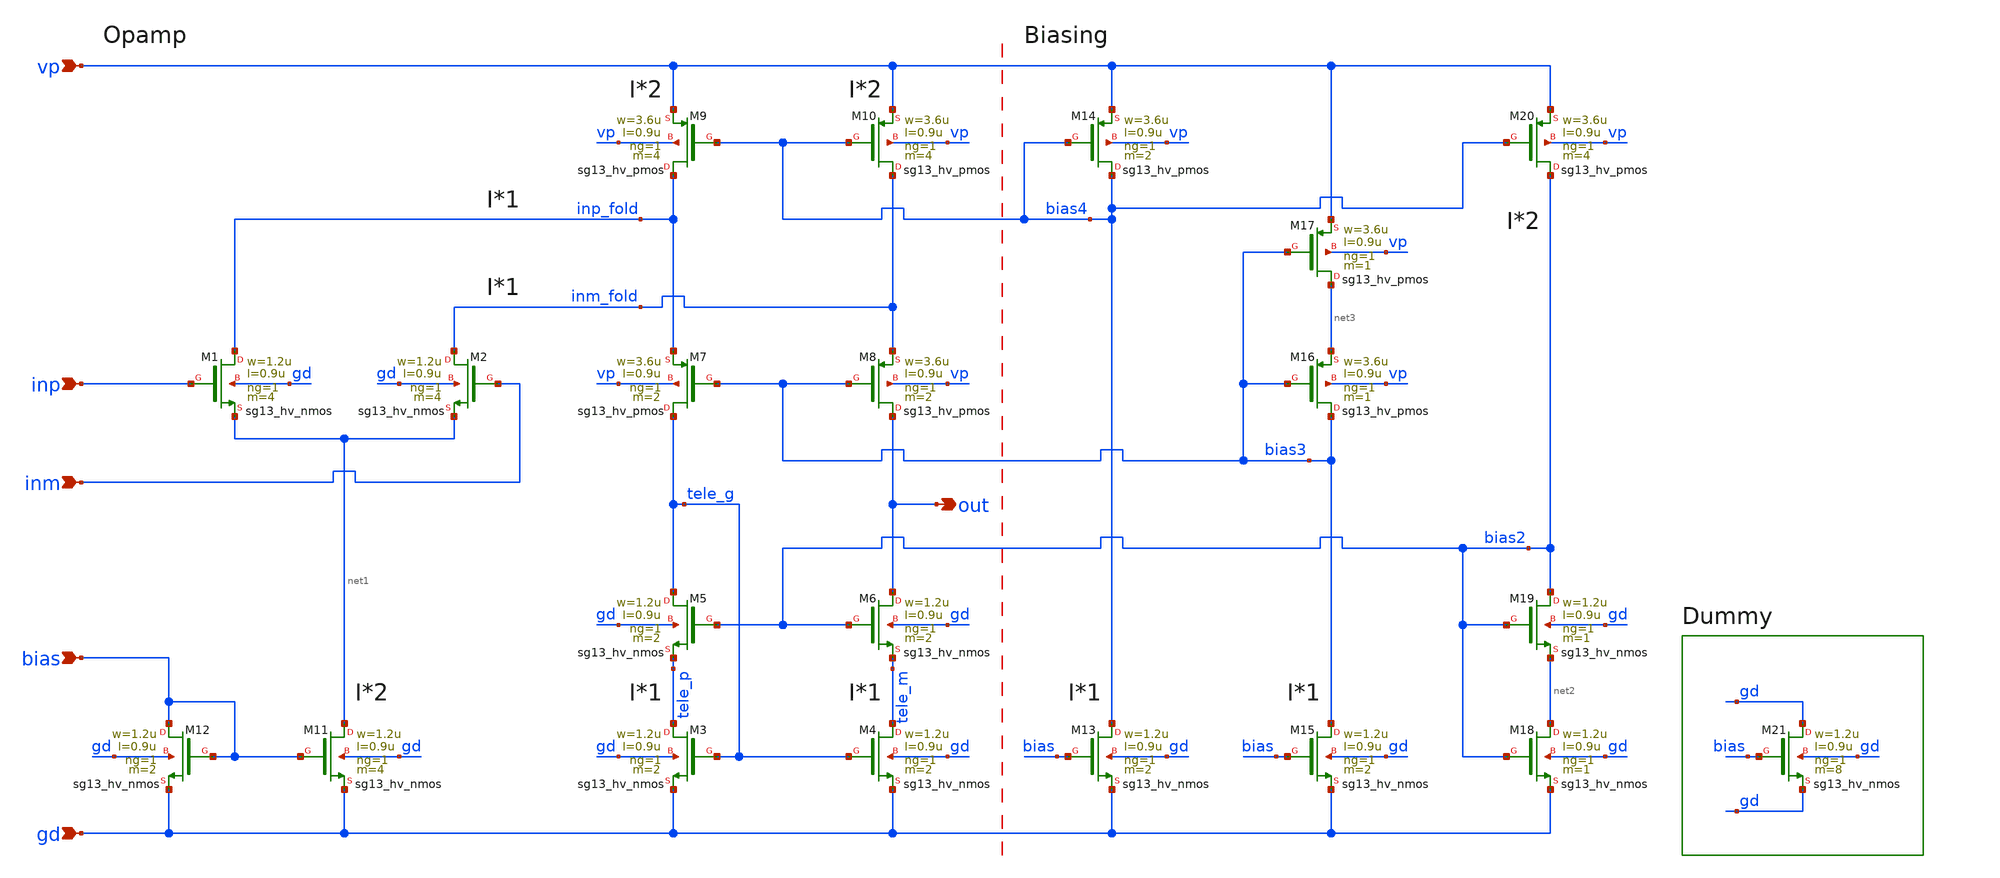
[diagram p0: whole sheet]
** sch_path: bandgap_res/opamp_folded.sch
**.subckt opamp_folded bias out vp inp inm gd
*.ipin bias
*.opin out
*.ipin vp
*.ipin inp
*.ipin inm
*.ipin gd
XM1 inp_fold inp net1 gd sg13_hv_nmos w=1.2u l=0.9u ng=1 m=4 mm_ok=1
XM2 inm_fold inm net1 gd sg13_hv_nmos w=1.2u l=0.9u ng=1 m=4 mm_ok=1
XM3 tele_p tele_g gd gd sg13_hv_nmos w=1.2u l=0.9u ng=1 m=2 mm_ok=1
XM4 tele_m tele_g gd gd sg13_hv_nmos w=1.2u l=0.9u ng=1 m=2 mm_ok=1
XM5 tele_g bias2 tele_p gd sg13_hv_nmos w=1.2u l=0.9u ng=1 m=2 mm_ok=1
XM6 out bias2 tele_m gd sg13_hv_nmos w=1.2u l=0.9u ng=1 m=2 mm_ok=1
XM7 tele_g bias3 inp_fold vp sg13_hv_pmos w=3.6u l=0.9u ng=1 m=2 mm_ok=1
XM8 out bias3 inm_fold vp sg13_hv_pmos w=3.6u l=0.9u ng=1 m=2 mm_ok=1
XM9 inp_fold bias4 vp vp sg13_hv_pmos w=3.6u l=0.9u ng=1 m=4 mm_ok=1
XM10 inm_fold bias4 vp vp sg13_hv_pmos w=3.6u l=0.9u ng=1 m=4 mm_ok=1
XM11 net1 bias gd gd sg13_hv_nmos w=1.2u l=0.9u ng=1 m=4 mm_ok=1
XM12 bias bias gd gd sg13_hv_nmos w=1.2u l=0.9u ng=1 m=2 mm_ok=1
XM13 bias4 bias gd gd sg13_hv_nmos w=1.2u l=0.9u ng=1 m=2 mm_ok=1
XM14 bias4 bias4 vp vp sg13_hv_pmos w=3.6u l=0.9u ng=1 m=2 mm_ok=1
XM15 bias3 bias gd gd sg13_hv_nmos w=1.2u l=0.9u ng=1 m=2 mm_ok=1
XM16 bias3 bias3 net3 vp sg13_hv_pmos w=3.6u l=0.9u ng=1 m=1 mm_ok=1
XM17 net3 bias3 vp vp sg13_hv_pmos w=3.6u l=0.9u ng=1 m=1 mm_ok=1
XM18 net2 bias2 gd gd sg13_hv_nmos w=1.2u l=0.9u ng=1 m=1 mm_ok=1
XM19 bias2 bias2 net2 gd sg13_hv_nmos w=1.2u l=0.9u ng=1 m=1 mm_ok=1
XM20 bias2 bias4 vp vp sg13_hv_pmos w=3.6u l=0.9u ng=1 m=4 mm_ok=1
XM21 gd bias gd gd sg13_hv_nmos w=1.2u l=0.9u ng=1 m=8 mm_ok=1
**.ends
.end
